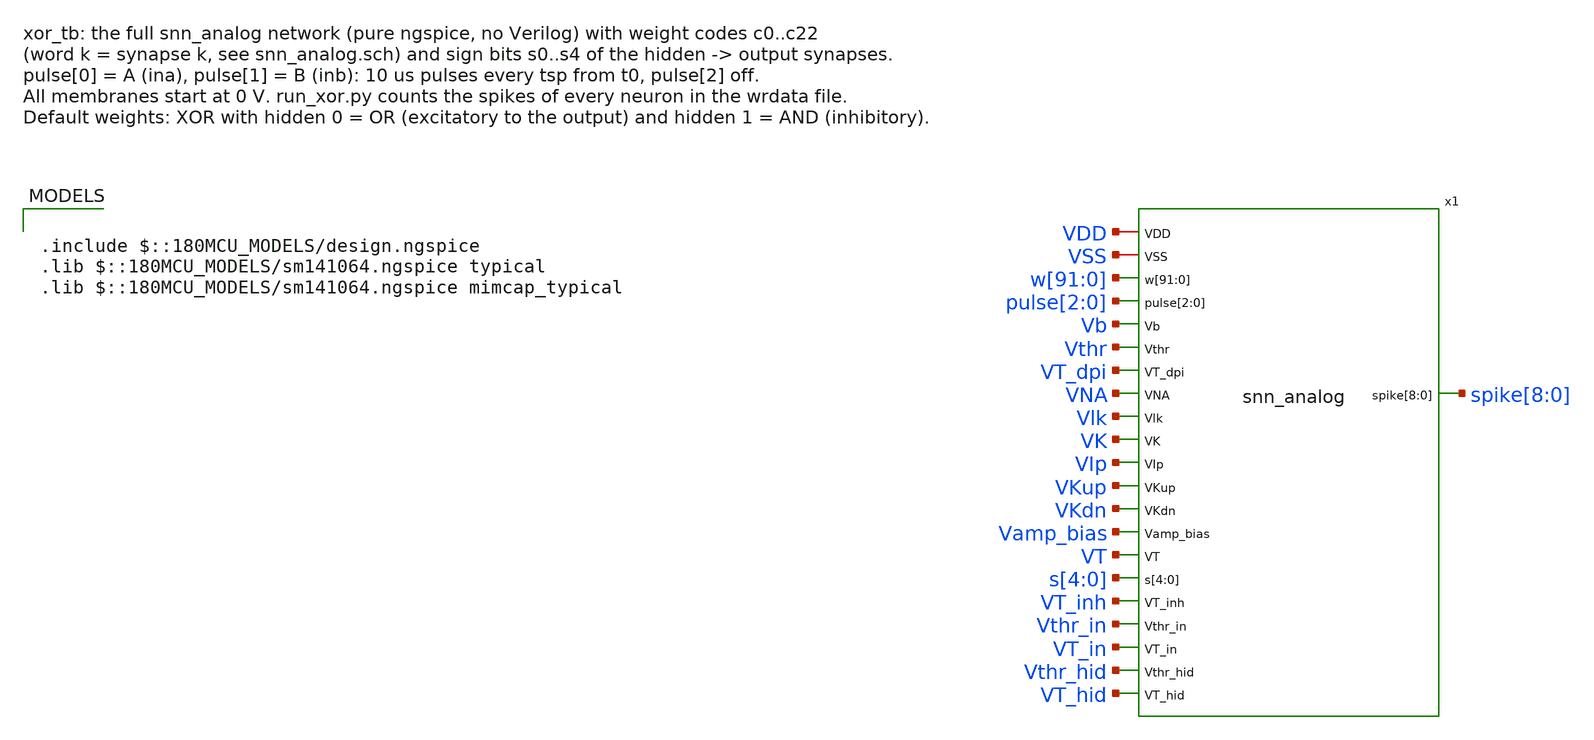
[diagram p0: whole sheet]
** sch_path: analog/testbenches/xor/xor_tb.sch
**.subckt xor_tb
x1 VDD VSS w[91] w[90] w[89] w[88] w[87] w[86] w[85] w[84] w[83] w[82] w[81] w[80] w[79] w[78] w[77]
+ w[76] w[75] w[74] w[73] w[72] w[71] w[70] w[69] w[68] w[67] w[66] w[65] w[64] w[63] w[62] w[61] w[60]
+ w[59] w[58] w[57] w[56] w[55] w[54] w[53] w[52] w[51] w[50] w[49] w[48] w[47] w[46] w[45] w[44] w[43]
+ w[42] w[41] w[40] w[39] w[38] w[37] w[36] w[35] w[34] w[33] w[32] w[31] w[30] w[29] w[28] w[27] w[26]
+ w[25] w[24] w[23] w[22] w[21] w[20] w[19] w[18] w[17] w[16] w[15] w[14] w[13] w[12] w[11] w[10] w[9] w[8]
+ w[7] w[6] w[5] w[4] w[3] w[2] w[1] w[0] pulse[2] pulse[1] pulse[0] Vb Vthr VT_dpi VNA Vlk VK VIp VKup
+ VKdn Vamp_bias VT s[4] s[3] s[2] s[1] s[0] VT_inh Vthr_in VT_in Vthr_hid VT_hid spike[8] spike[7]
+ spike[6] spike[5] spike[4] spike[3] spike[2] spike[1] spike[0] snn_analog
**** begin user architecture code

.include $::180MCU_MODELS/design.ngspice
.lib $::180MCU_MODELS/sm141064.ngspice typical
.lib $::180MCU_MODELS/sm141064.ngspice mimcap_typical


.param vdd=3.3 p_vthr=2.785 p_vtau=0.5096 p_vtau_i=0.5096 iref=14.42n
.param p_vthr_in=2.4 p_vtau_in=0.72 p_vthr_hid=2.5 p_vtau_hid=0.6225
.param p_vlk=0.48 p_vamp_bias=0.535 p_vip=0.573 p_vna=1.93 p_vkup=2.35 p_vk=1.22 p_vkdn=0.588
+ p_vt=1.66
* Weight codes (DAC branch weights 1:2:3:4: code 15 = weight 10, code 8 = 4, code 1 = 1)
* in -> input relay: words 0, 1; input i -> hidden j: word 3 + 3j + i; hidden j -> output: 18 + j
.param c0=15 c1=15 c2=0 c3=15 c4=15 c5=0 c6=1 c7=1 c8=0 c9=0 c10=0 c11=0 c12=0 c13=0 c14=0 c15=0
+ c16=0 c17=0 c18=1 c19=15 c20=0 c21=0 c22=0
.param s0=0 s1=1 s2=0 s3=0 s4=0
.param ina=1 inb=1 tpw=10u tsp=200u t0=100u tstop=4.1m
.csparam tstop_c={tstop}
Vdd VDD 0 {vdd}
Vss VSS 0 0
* DAC unit current: Iref into a diode-connected unit current source (w[0] = 15 nA)
Iref VDD Vb {iref}
XMref Vb Vb 0 0 nfet_03v3 L=8u W=1u nf=1
Vthr Vthr 0 {p_vthr}
Vtau VDD VT_dpi {p_vtau}
Vtau_i VDD VT_inh {p_vtau_i}
VNA VNA VSS {p_vna}
Vlk Vlk VSS {p_vlk}
VK VK VSS {p_vk}
VIp VIp VSS {p_vip}
VKup VKup VSS {p_vkup}
VKdn VKdn VSS {p_vkdn}
Vamp_bias Vamp_bias VSS {p_vamp_bias}
VT VT VSS {p_vt}
Vthr_in Vthr_in 0 {p_vthr_in}
Vtau_in VDD VT_in {p_vtau_in}
Vthr_hid Vthr_hid 0 {p_vthr_hid}
Vtau_hid VDD VT_hid {p_vtau_hid}
Vw0 w[0] 0 {vdd*(floor(c0/1)-2*floor(c0/2))}
Vw1 w[1] 0 {vdd*(floor(c0/2)-2*floor(c0/4))}
Vw2 w[2] 0 {vdd*(floor(c0/4)-2*floor(c0/8))}
Vw3 w[3] 0 {vdd*(floor(c0/8)-2*floor(c0/16))}
Vw4 w[4] 0 {vdd*(floor(c1/1)-2*floor(c1/2))}
Vw5 w[5] 0 {vdd*(floor(c1/2)-2*floor(c1/4))}
Vw6 w[6] 0 {vdd*(floor(c1/4)-2*floor(c1/8))}
Vw7 w[7] 0 {vdd*(floor(c1/8)-2*floor(c1/16))}
Vw8 w[8] 0 {vdd*(floor(c2/1)-2*floor(c2/2))}
Vw9 w[9] 0 {vdd*(floor(c2/2)-2*floor(c2/4))}
Vw10 w[10] 0 {vdd*(floor(c2/4)-2*floor(c2/8))}
Vw11 w[11] 0 {vdd*(floor(c2/8)-2*floor(c2/16))}
Vw12 w[12] 0 {vdd*(floor(c3/1)-2*floor(c3/2))}
Vw13 w[13] 0 {vdd*(floor(c3/2)-2*floor(c3/4))}
Vw14 w[14] 0 {vdd*(floor(c3/4)-2*floor(c3/8))}
Vw15 w[15] 0 {vdd*(floor(c3/8)-2*floor(c3/16))}
Vw16 w[16] 0 {vdd*(floor(c4/1)-2*floor(c4/2))}
Vw17 w[17] 0 {vdd*(floor(c4/2)-2*floor(c4/4))}
Vw18 w[18] 0 {vdd*(floor(c4/4)-2*floor(c4/8))}
Vw19 w[19] 0 {vdd*(floor(c4/8)-2*floor(c4/16))}
Vw20 w[20] 0 {vdd*(floor(c5/1)-2*floor(c5/2))}
Vw21 w[21] 0 {vdd*(floor(c5/2)-2*floor(c5/4))}
Vw22 w[22] 0 {vdd*(floor(c5/4)-2*floor(c5/8))}
Vw23 w[23] 0 {vdd*(floor(c5/8)-2*floor(c5/16))}
Vw24 w[24] 0 {vdd*(floor(c6/1)-2*floor(c6/2))}
Vw25 w[25] 0 {vdd*(floor(c6/2)-2*floor(c6/4))}
Vw26 w[26] 0 {vdd*(floor(c6/4)-2*floor(c6/8))}
Vw27 w[27] 0 {vdd*(floor(c6/8)-2*floor(c6/16))}
Vw28 w[28] 0 {vdd*(floor(c7/1)-2*floor(c7/2))}
Vw29 w[29] 0 {vdd*(floor(c7/2)-2*floor(c7/4))}
Vw30 w[30] 0 {vdd*(floor(c7/4)-2*floor(c7/8))}
Vw31 w[31] 0 {vdd*(floor(c7/8)-2*floor(c7/16))}
Vw32 w[32] 0 {vdd*(floor(c8/1)-2*floor(c8/2))}
Vw33 w[33] 0 {vdd*(floor(c8/2)-2*floor(c8/4))}
Vw34 w[34] 0 {vdd*(floor(c8/4)-2*floor(c8/8))}
Vw35 w[35] 0 {vdd*(floor(c8/8)-2*floor(c8/16))}
Vw36 w[36] 0 {vdd*(floor(c9/1)-2*floor(c9/2))}
Vw37 w[37] 0 {vdd*(floor(c9/2)-2*floor(c9/4))}
Vw38 w[38] 0 {vdd*(floor(c9/4)-2*floor(c9/8))}
Vw39 w[39] 0 {vdd*(floor(c9/8)-2*floor(c9/16))}
Vw40 w[40] 0 {vdd*(floor(c10/1)-2*floor(c10/2))}
Vw41 w[41] 0 {vdd*(floor(c10/2)-2*floor(c10/4))}
Vw42 w[42] 0 {vdd*(floor(c10/4)-2*floor(c10/8))}
Vw43 w[43] 0 {vdd*(floor(c10/8)-2*floor(c10/16))}
Vw44 w[44] 0 {vdd*(floor(c11/1)-2*floor(c11/2))}
Vw45 w[45] 0 {vdd*(floor(c11/2)-2*floor(c11/4))}
Vw46 w[46] 0 {vdd*(floor(c11/4)-2*floor(c11/8))}
Vw47 w[47] 0 {vdd*(floor(c11/8)-2*floor(c11/16))}
Vw48 w[48] 0 {vdd*(floor(c12/1)-2*floor(c12/2))}
Vw49 w[49] 0 {vdd*(floor(c12/2)-2*floor(c12/4))}
Vw50 w[50] 0 {vdd*(floor(c12/4)-2*floor(c12/8))}
Vw51 w[51] 0 {vdd*(floor(c12/8)-2*floor(c12/16))}
Vw52 w[52] 0 {vdd*(floor(c13/1)-2*floor(c13/2))}
Vw53 w[53] 0 {vdd*(floor(c13/2)-2*floor(c13/4))}
Vw54 w[54] 0 {vdd*(floor(c13/4)-2*floor(c13/8))}
Vw55 w[55] 0 {vdd*(floor(c13/8)-2*floor(c13/16))}
Vw56 w[56] 0 {vdd*(floor(c14/1)-2*floor(c14/2))}
Vw57 w[57] 0 {vdd*(floor(c14/2)-2*floor(c14/4))}
Vw58 w[58] 0 {vdd*(floor(c14/4)-2*floor(c14/8))}
Vw59 w[59] 0 {vdd*(floor(c14/8)-2*floor(c14/16))}
Vw60 w[60] 0 {vdd*(floor(c15/1)-2*floor(c15/2))}
Vw61 w[61] 0 {vdd*(floor(c15/2)-2*floor(c15/4))}
Vw62 w[62] 0 {vdd*(floor(c15/4)-2*floor(c15/8))}
Vw63 w[63] 0 {vdd*(floor(c15/8)-2*floor(c15/16))}
Vw64 w[64] 0 {vdd*(floor(c16/1)-2*floor(c16/2))}
Vw65 w[65] 0 {vdd*(floor(c16/2)-2*floor(c16/4))}
Vw66 w[66] 0 {vdd*(floor(c16/4)-2*floor(c16/8))}
Vw67 w[67] 0 {vdd*(floor(c16/8)-2*floor(c16/16))}
Vw68 w[68] 0 {vdd*(floor(c17/1)-2*floor(c17/2))}
Vw69 w[69] 0 {vdd*(floor(c17/2)-2*floor(c17/4))}
Vw70 w[70] 0 {vdd*(floor(c17/4)-2*floor(c17/8))}
Vw71 w[71] 0 {vdd*(floor(c17/8)-2*floor(c17/16))}
Vw72 w[72] 0 {vdd*(floor(c18/1)-2*floor(c18/2))}
Vw73 w[73] 0 {vdd*(floor(c18/2)-2*floor(c18/4))}
Vw74 w[74] 0 {vdd*(floor(c18/4)-2*floor(c18/8))}
Vw75 w[75] 0 {vdd*(floor(c18/8)-2*floor(c18/16))}
Vw76 w[76] 0 {vdd*(floor(c19/1)-2*floor(c19/2))}
Vw77 w[77] 0 {vdd*(floor(c19/2)-2*floor(c19/4))}
Vw78 w[78] 0 {vdd*(floor(c19/4)-2*floor(c19/8))}
Vw79 w[79] 0 {vdd*(floor(c19/8)-2*floor(c19/16))}
Vw80 w[80] 0 {vdd*(floor(c20/1)-2*floor(c20/2))}
Vw81 w[81] 0 {vdd*(floor(c20/2)-2*floor(c20/4))}
Vw82 w[82] 0 {vdd*(floor(c20/4)-2*floor(c20/8))}
Vw83 w[83] 0 {vdd*(floor(c20/8)-2*floor(c20/16))}
Vw84 w[84] 0 {vdd*(floor(c21/1)-2*floor(c21/2))}
Vw85 w[85] 0 {vdd*(floor(c21/2)-2*floor(c21/4))}
Vw86 w[86] 0 {vdd*(floor(c21/4)-2*floor(c21/8))}
Vw87 w[87] 0 {vdd*(floor(c21/8)-2*floor(c21/16))}
Vw88 w[88] 0 {vdd*(floor(c22/1)-2*floor(c22/2))}
Vw89 w[89] 0 {vdd*(floor(c22/2)-2*floor(c22/4))}
Vw90 w[90] 0 {vdd*(floor(c22/4)-2*floor(c22/8))}
Vw91 w[91] 0 {vdd*(floor(c22/8)-2*floor(c22/16))}
Vs0 s[0] 0 {vdd*s0}
Vs1 s[1] 0 {vdd*s1}
Vs2 s[2] 0 {vdd*s2}
Vs3 s[3] 0 {vdd*s3}
Vs4 s[4] 0 {vdd*s4}
Vp0 pulse[0] 0 pulse(0 {vdd*ina} {t0} 10n 10n {tpw} {tsp})
Vp1 pulse[1] 0 pulse(0 {vdd*inb} {t0} 10n 10n {tpw} {tsp})
Vp2 pulse[2] 0 0
* spike[n] copied to sp<n> (no load) for wrdata
Esp0 sp0 0 spike[0] 0 1
Esp1 sp1 0 spike[1] 0 1
Esp2 sp2 0 spike[2] 0 1
Esp3 sp3 0 spike[3] 0 1
Esp4 sp4 0 spike[4] 0 1
Esp5 sp5 0 spike[5] 0 1
Esp6 sp6 0 spike[6] 0 1
Esp7 sp7 0 spike[7] 0 1
Esp8 sp8 0 spike[8] 0 1
.ic v(x1.VMEM_0)=0 v(x1.VMEM_1)=0 v(x1.VMEM_2)=0 v(x1.VMEM_3)=0 v(x1.VMEM_4)=0 v(x1.VMEM_5)=0
+ v(x1.VMEM_6)=0 v(x1.VMEM_7)=0 v(x1.VMEM_8)=0 v(spike[0])=0 v(spike[1])=0 v(spike[2])=0 v(spike[3])=0 v(spike[4])=0
+ v(spike[5])=0 v(spike[6])=0 v(spike[7])=0 v(spike[8])=0
.options method=gear

.control
  save v(sp0) v(sp1) v(sp2) v(sp3) v(sp4) v(sp5) v(sp6) v(sp7) v(sp8) v(x1.VMEM_8) v(x1.VMEM_3)
+ v(x1.VMEM_4)
  set wr_singlescale
  set wr_vecnames
  * Max step 0.1u: at 0.5u a relay spike edge sometimes kicked this neuron into a false spike
  tran 0.1u $&tstop_c 0 0.1u
  meas tran vmax_out max v(x1.VMEM_8)
  echo RES vmax_out=$&vmax_out
  wrdata xor_tb.txt v(sp0) v(sp1) v(sp2) v(sp3) v(sp4) v(sp5) v(sp6) v(sp7) v(sp8) v(x1.VMEM_8)
+ v(x1.VMEM_3) v(x1.VMEM_4)
  if $?batchmode = 0
    plot v(x1.VMEM_8) v(sp8)+4 v(sp3)*0.3+8 v(sp4)*0.3+9.5 v(sp0)*0.3+11 v(sp1)*0.3+12.5 title 'Output membrane, output spike; hidden OR, AND; inputs A, B (offset)'
+ ylabel 'V'
  end
.endc


**** end user architecture code
**.ends
.end
